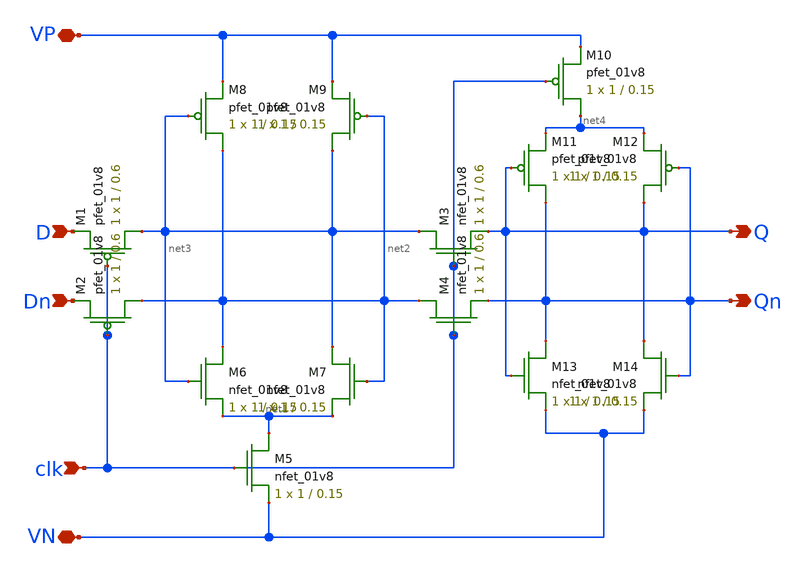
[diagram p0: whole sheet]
** sch_path: DRAM_Components/Schematic/CSRLDFF.sch
**.subckt CSRLDFF D clk VN Q Qn Dn VP
*.ipin D
*.ipin clk
*.iopin VN
*.opin Q
*.opin Qn
*.ipin Dn
*.iopin VP
XM1 net3 clk D VP sky130_fd_pr__pfet_01v8 L=0.6 W=1 nf=1 ad='int((nf+1)/2) * W/nf * 0.29' as='int((nf+2)/2) * W/nf * 0.29'
+ pd='2*int((nf+1)/2) * (W/nf + 0.29)' ps='2*int((nf+2)/2) * (W/nf + 0.29)' nrd='0.29 / W' nrs='0.29 / W'
+ sa=0 sb=0 sd=0 mult=1 m=1
XM2 net2 clk Dn VP sky130_fd_pr__pfet_01v8 L=0.6 W=1 nf=1 ad='int((nf+1)/2) * W/nf * 0.29' as='int((nf+2)/2) * W/nf * 0.29'
+ pd='2*int((nf+1)/2) * (W/nf + 0.29)' ps='2*int((nf+2)/2) * (W/nf + 0.29)' nrd='0.29 / W' nrs='0.29 / W'
+ sa=0 sb=0 sd=0 mult=1 m=1
XM3 net3 clk Q VN sky130_fd_pr__nfet_01v8 L=0.6 W=1 nf=1 ad='int((nf+1)/2) * W/nf * 0.29' as='int((nf+2)/2) * W/nf * 0.29'
+ pd='2*int((nf+1)/2) * (W/nf + 0.29)' ps='2*int((nf+2)/2) * (W/nf + 0.29)' nrd='0.29 / W' nrs='0.29 / W'
+ sa=0 sb=0 sd=0 mult=1 m=1
XM4 net2 clk Qn VN sky130_fd_pr__nfet_01v8 L=0.6 W=1 nf=1 ad='int((nf+1)/2) * W/nf * 0.29' as='int((nf+2)/2) * W/nf * 0.29'
+ pd='2*int((nf+1)/2) * (W/nf + 0.29)' ps='2*int((nf+2)/2) * (W/nf + 0.29)' nrd='0.29 / W' nrs='0.29 / W'
+ sa=0 sb=0 sd=0 mult=1 m=1
XM5 net1 clk VN VN sky130_fd_pr__nfet_01v8 L=0.15 W=1 nf=1 ad='int((nf+1)/2) * W/nf * 0.29' as='int((nf+2)/2) * W/nf * 0.29'
+ pd='2*int((nf+1)/2) * (W/nf + 0.29)' ps='2*int((nf+2)/2) * (W/nf + 0.29)' nrd='0.29 / W' nrs='0.29 / W'
+ sa=0 sb=0 sd=0 mult=1 m=1
XM6 net2 net3 net1 VN sky130_fd_pr__nfet_01v8 L=0.15 W=1 nf=1 ad='int((nf+1)/2) * W/nf * 0.29' as='int((nf+2)/2) * W/nf * 0.29'
+ pd='2*int((nf+1)/2) * (W/nf + 0.29)' ps='2*int((nf+2)/2) * (W/nf + 0.29)' nrd='0.29 / W' nrs='0.29 / W'
+ sa=0 sb=0 sd=0 mult=1 m=1
XM7 net3 net2 net1 VN sky130_fd_pr__nfet_01v8 L=0.15 W=1 nf=1 ad='int((nf+1)/2) * W/nf * 0.29' as='int((nf+2)/2) * W/nf * 0.29'
+ pd='2*int((nf+1)/2) * (W/nf + 0.29)' ps='2*int((nf+2)/2) * (W/nf + 0.29)' nrd='0.29 / W' nrs='0.29 / W'
+ sa=0 sb=0 sd=0 mult=1 m=1
XM8 net2 net3 VP VP sky130_fd_pr__pfet_01v8 L=0.15 W=1 nf=1 ad='int((nf+1)/2) * W/nf * 0.29' as='int((nf+2)/2) * W/nf * 0.29'
+ pd='2*int((nf+1)/2) * (W/nf + 0.29)' ps='2*int((nf+2)/2) * (W/nf + 0.29)' nrd='0.29 / W' nrs='0.29 / W'
+ sa=0 sb=0 sd=0 mult=1 m=1
XM9 net3 net2 VP VP sky130_fd_pr__pfet_01v8 L=0.15 W=1 nf=1 ad='int((nf+1)/2) * W/nf * 0.29' as='int((nf+2)/2) * W/nf * 0.29'
+ pd='2*int((nf+1)/2) * (W/nf + 0.29)' ps='2*int((nf+2)/2) * (W/nf + 0.29)' nrd='0.29 / W' nrs='0.29 / W'
+ sa=0 sb=0 sd=0 mult=1 m=1
XM10 net4 clk VP VP sky130_fd_pr__pfet_01v8 L=0.15 W=1 nf=1 ad='int((nf+1)/2) * W/nf * 0.29' as='int((nf+2)/2) * W/nf * 0.29'
+ pd='2*int((nf+1)/2) * (W/nf + 0.29)' ps='2*int((nf+2)/2) * (W/nf + 0.29)' nrd='0.29 / W' nrs='0.29 / W'
+ sa=0 sb=0 sd=0 mult=1 m=1
XM11 Qn Q net4 VP sky130_fd_pr__pfet_01v8 L=0.15 W=1 nf=1 ad='int((nf+1)/2) * W/nf * 0.29' as='int((nf+2)/2) * W/nf * 0.29'
+ pd='2*int((nf+1)/2) * (W/nf + 0.29)' ps='2*int((nf+2)/2) * (W/nf + 0.29)' nrd='0.29 / W' nrs='0.29 / W'
+ sa=0 sb=0 sd=0 mult=1 m=1
XM12 Q Qn net4 VP sky130_fd_pr__pfet_01v8 L=0.15 W=1 nf=1 ad='int((nf+1)/2) * W/nf * 0.29' as='int((nf+2)/2) * W/nf * 0.29'
+ pd='2*int((nf+1)/2) * (W/nf + 0.29)' ps='2*int((nf+2)/2) * (W/nf + 0.29)' nrd='0.29 / W' nrs='0.29 / W'
+ sa=0 sb=0 sd=0 mult=1 m=1
XM13 Qn Q VN VN sky130_fd_pr__nfet_01v8 L=0.15 W=1 nf=1 ad='int((nf+1)/2) * W/nf * 0.29' as='int((nf+2)/2) * W/nf * 0.29'
+ pd='2*int((nf+1)/2) * (W/nf + 0.29)' ps='2*int((nf+2)/2) * (W/nf + 0.29)' nrd='0.29 / W' nrs='0.29 / W'
+ sa=0 sb=0 sd=0 mult=1 m=1
XM14 Q Qn VN VN sky130_fd_pr__nfet_01v8 L=0.15 W=1 nf=1 ad='int((nf+1)/2) * W/nf * 0.29' as='int((nf+2)/2) * W/nf * 0.29'
+ pd='2*int((nf+1)/2) * (W/nf + 0.29)' ps='2*int((nf+2)/2) * (W/nf + 0.29)' nrd='0.29 / W' nrs='0.29 / W'
+ sa=0 sb=0 sd=0 mult=1 m=1
**.ends
.end
